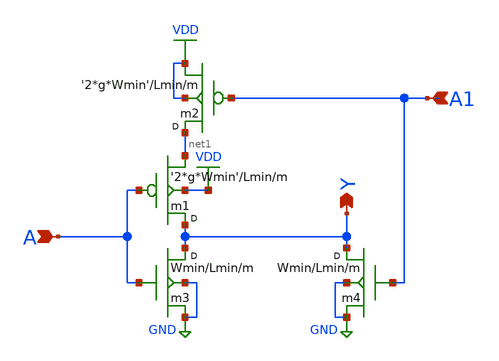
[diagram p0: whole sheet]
** sch_path: Sources/crafted/nor2.sch
**.subckt nor2 A Y A1
*.ipin A
*.opin Y
*.ipin A1
m3 Y A GND GND nmos4 w=Wmin l=Lmin m=m
m1 Y A net1 VDD pmos4 w='2*g*Wmin' l=Lmin m=m
m4 Y A1 GND GND nmos4 w=Wmin l=Lmin m=m
m2 net1 A1 VDD VDD pmos4 w='2*g*Wmin' l=Lmin m=m
**.ends
.GLOBAL VDD
.GLOBAL GND
.end
